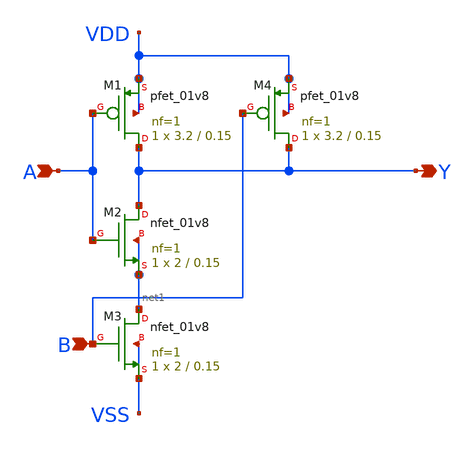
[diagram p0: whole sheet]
** sch_path: design/xschem/NAND/nand2.sch
**.subckt nand2 A Y B
*.ipin A
*.opin Y
*.ipin B
XM1 Y A VDD VDD sky130_fd_pr__pfet_01v8 L=0.15 W=3.2 nf=1 ad='int((nf+1)/2) * W/nf * 0.29' as='int((nf+2)/2) * W/nf * 0.29'
+ pd='2*int((nf+1)/2) * (W/nf + 0.29)' ps='2*int((nf+2)/2) * (W/nf + 0.29)' nrd='0.29 / W' nrs='0.29 / W'
+ sa=0 sb=0 sd=0 mult=1 m=1
XM2 Y A net1 net1 sky130_fd_pr__nfet_01v8 L=0.15 W=2 nf=1 ad='int((nf+1)/2) * W/nf * 0.29' as='int((nf+2)/2) * W/nf * 0.29'
+ pd='2*int((nf+1)/2) * (W/nf + 0.29)' ps='2*int((nf+2)/2) * (W/nf + 0.29)' nrd='0.29 / W' nrs='0.29 / W'
+ sa=0 sb=0 sd=0 mult=1 m=1
XM3 net1 B VSS VSS sky130_fd_pr__nfet_01v8 L=0.15 W=2 nf=1 ad='int((nf+1)/2) * W/nf * 0.29' as='int((nf+2)/2) * W/nf * 0.29'
+ pd='2*int((nf+1)/2) * (W/nf + 0.29)' ps='2*int((nf+2)/2) * (W/nf + 0.29)' nrd='0.29 / W' nrs='0.29 / W'
+ sa=0 sb=0 sd=0 mult=1 m=1
XM4 Y B VDD VDD sky130_fd_pr__pfet_01v8 L=0.15 W=3.2 nf=1 ad='int((nf+1)/2) * W/nf * 0.29' as='int((nf+2)/2) * W/nf * 0.29'
+ pd='2*int((nf+1)/2) * (W/nf + 0.29)' ps='2*int((nf+2)/2) * (W/nf + 0.29)' nrd='0.29 / W' nrs='0.29 / W'
+ sa=0 sb=0 sd=0 mult=1 m=1
**.ends
.end
